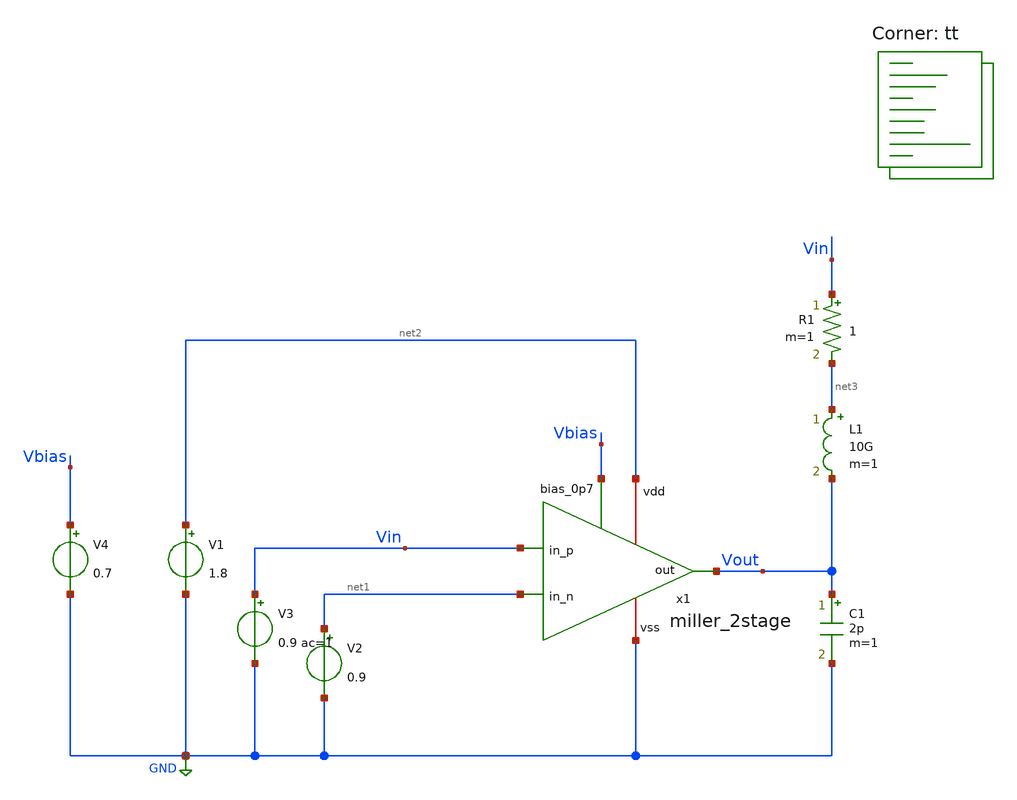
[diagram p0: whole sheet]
** sch_path: xschem/ip_block/opamp/miller_2stage/tb_miller_2stage.sch
**.subckt tb_miller_2stage
V1 net2 GND 1.8
V2 net1 GND 0.9
V3 Vin GND 0.9 ac=1
C1 Vout GND 2p m=1
L1 net3 Vout 10G m=1
R1 Vin net3 1 m=1
V4 Vbias GND 0.7
x1 net2 net1 Vin Vout Vbias GND miller_2stage
**** begin user architecture code


.param temp=27

.op
.ac dec 10 1 1G
*.tran 0.001 50n 20n

.control
ac dec 10 1 1G
let phase = 180/PI*vp(Vout)

plot vdb(Vout) phase
plot phase

.endc

.save all



.lib $::SKYWATER_MODELS/sky130.lib.spice tt
**** end user architecture code
**.ends
.GLOBAL GND
.end
